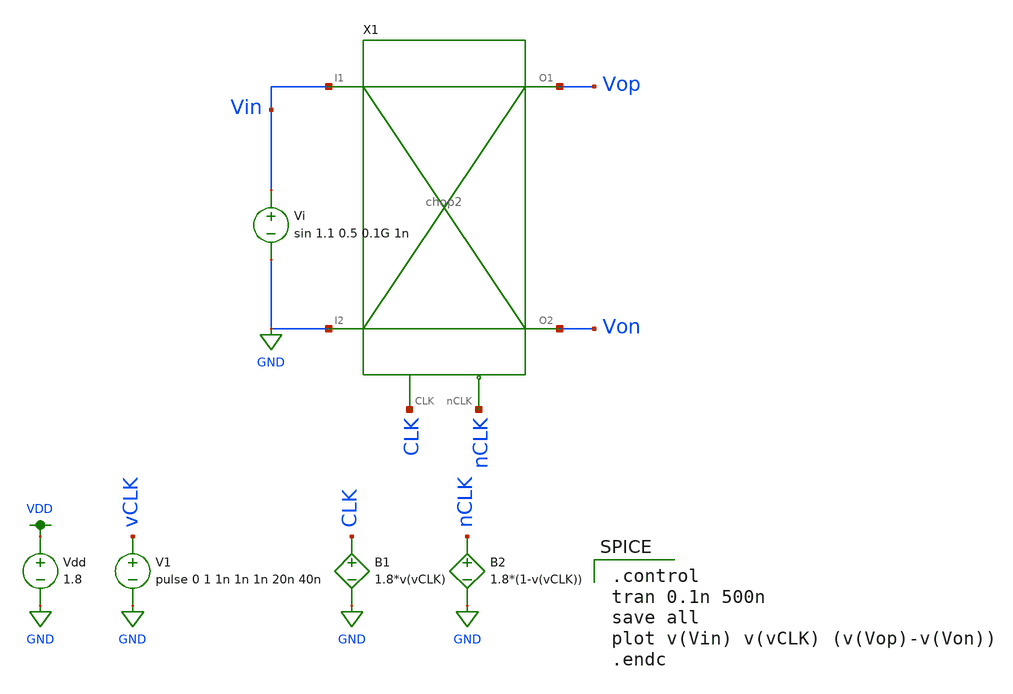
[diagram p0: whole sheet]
** sch_path: schematic/test/chop2_test.sch
**.subckt chop2_test
V1 vCLK GND pulse 0 1 1n 1n 1n 20n 40n
B1 CLK GND V=1.8*v(vCLK)
B2 nCLK GND V=1.8*(1-v(vCLK))
Vi Vin GND sin 1.1 0.5 0.1G 1n
Vdd VDD GND 1.8
X1 GND Vin Vop Von CLK nCLK chop2
**** begin user architecture code

.option wnflag=1
.param MC_SWITCH=0.0
.lib ~/skywater/skywater-pdk/libraries/sky130_fd_pr_ngspice/latest/models/sky130.lib.spice tt


.control
tran 0.1n 500n
save all
plot v(Vin) v(vCLK) (v(Vop)-v(Von))
.endc

**** end user architecture code
**.ends
.GLOBAL GND
.GLOBAL VDD
.end
